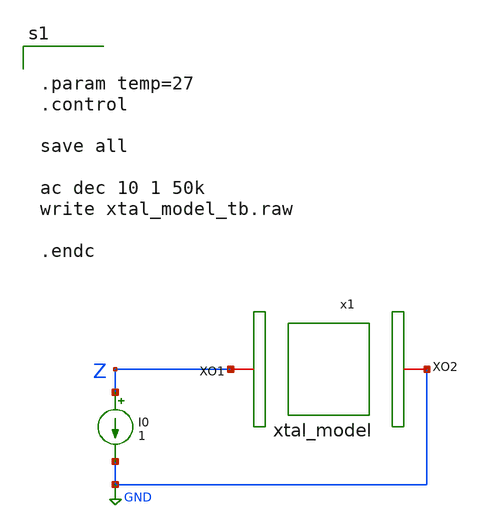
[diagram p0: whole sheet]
** sch_path: xtal_model_tb.sch
**.subckt xtal_model_tb
x1 Z GND xtal_model
I0 Z GND 1
**** begin user architecture code


.param temp=27
.control

save all

ac dec 10 1 50k
write xtal_model_tb.raw

.endc


**** end user architecture code
**.ends

* expanding   symbol:  /foss/designs/XTAL/xtal/xtal_model.sym # of pins=2
** sym_path: xtal_model.sym
** sch_path: xtal_model.sch
.subckt xtal_model XO1 XO2
*.iopin XO2
*.iopin XO1
Rs XO1 net1 50k m=1
Cs net1 net2 1.39f m=1
C0 XO1 XO2 1.35p m=1
Ls net2 XO2 17k m=1
.ends

.GLOBAL GND
.end
